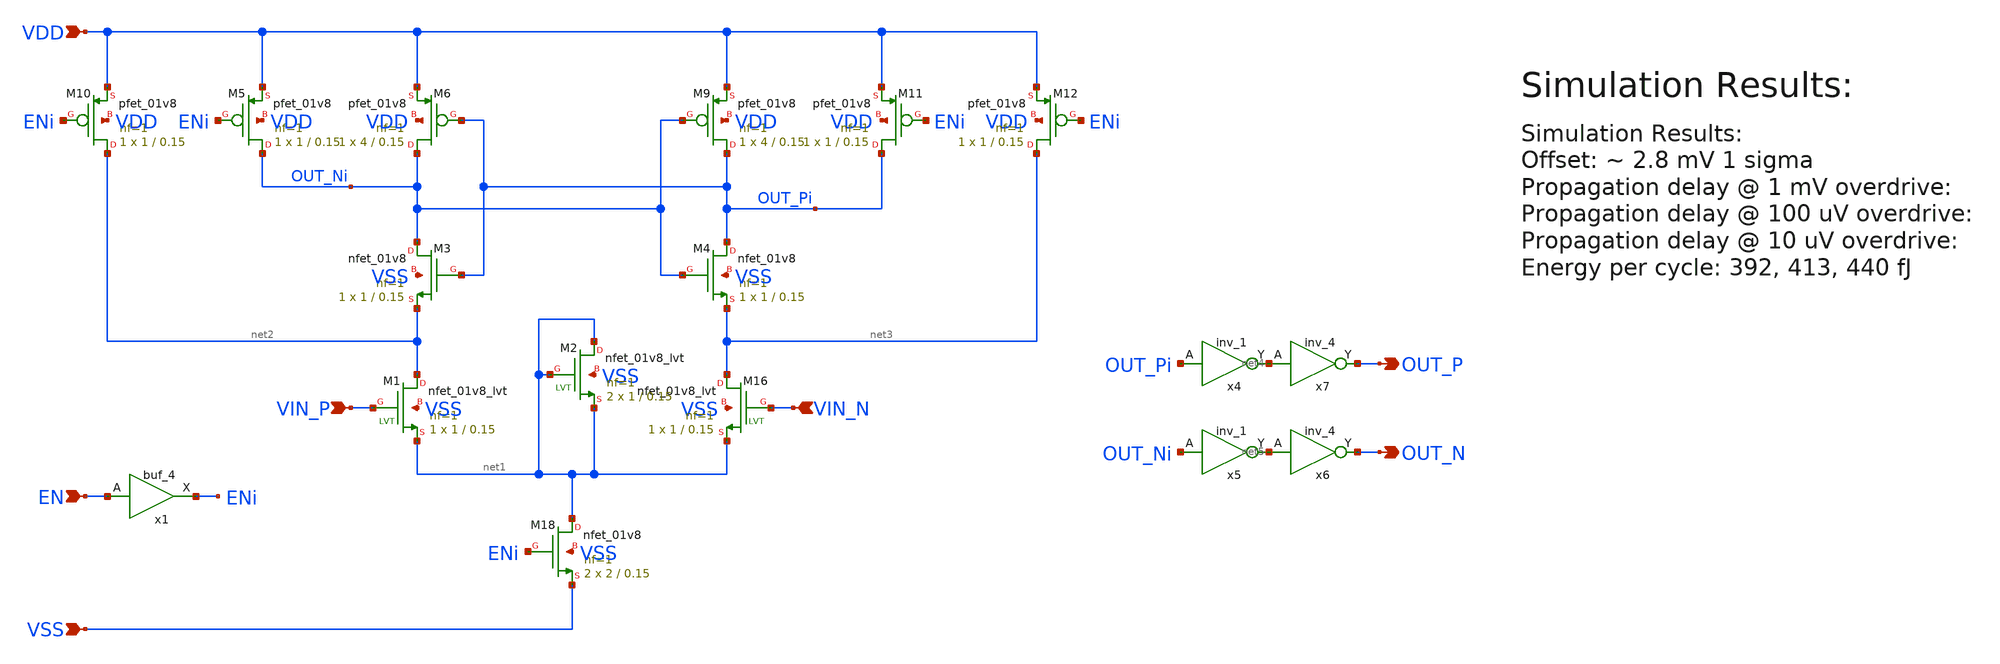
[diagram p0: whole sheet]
** sch_path: schematic/subcells/latched_comparator/latched_comparator.sch
**.subckt latched_comparator VIN_P VIN_N VDD VSS EN OUT_N OUT_P
*.ipin VIN_P
*.ipin VIN_N
*.ipin VDD
*.ipin VSS
*.ipin EN
*.opin OUT_N
*.opin OUT_P
x1 EN VSS VSS VDD VDD ENi sky130_fd_sc_hd__buf_4
XM10 net2 ENi VDD VDD sky130_fd_pr__pfet_01v8 L=0.15 W=1 nf=1 ad='int((nf+1)/2) * W/nf * 0.29' as='int((nf+2)/2) * W/nf * 0.29'
+ pd='2*int((nf+1)/2) * (W/nf + 0.29)' ps='2*int((nf+2)/2) * (W/nf + 0.29)' nrd='0.29 / W' nrs='0.29 / W'
+ sa=0 sb=0 sd=0 mult=1 m=1
XM5 OUT_Ni ENi VDD VDD sky130_fd_pr__pfet_01v8 L=0.15 W=1 nf=1 ad='int((nf+1)/2) * W/nf * 0.29' as='int((nf+2)/2) * W/nf * 0.29'
+ pd='2*int((nf+1)/2) * (W/nf + 0.29)' ps='2*int((nf+2)/2) * (W/nf + 0.29)' nrd='0.29 / W' nrs='0.29 / W'
+ sa=0 sb=0 sd=0 mult=1 m=1
XM6 OUT_Ni OUT_Pi VDD VDD sky130_fd_pr__pfet_01v8 L=0.15 W=4 nf=1 ad='int((nf+1)/2) * W/nf * 0.29' as='int((nf+2)/2) * W/nf * 0.29'
+ pd='2*int((nf+1)/2) * (W/nf + 0.29)' ps='2*int((nf+2)/2) * (W/nf + 0.29)' nrd='0.29 / W' nrs='0.29 / W'
+ sa=0 sb=0 sd=0 mult=1 m=1
XM9 OUT_Pi OUT_Ni VDD VDD sky130_fd_pr__pfet_01v8 L=0.15 W=4 nf=1 ad='int((nf+1)/2) * W/nf * 0.29' as='int((nf+2)/2) * W/nf * 0.29'
+ pd='2*int((nf+1)/2) * (W/nf + 0.29)' ps='2*int((nf+2)/2) * (W/nf + 0.29)' nrd='0.29 / W' nrs='0.29 / W'
+ sa=0 sb=0 sd=0 mult=1 m=1
XM3 OUT_Ni OUT_Pi net2 VSS sky130_fd_pr__nfet_01v8 L=0.15 W=1 nf=1 ad='int((nf+1)/2) * W/nf * 0.29' as='int((nf+2)/2) * W/nf * 0.29'
+ pd='2*int((nf+1)/2) * (W/nf + 0.29)' ps='2*int((nf+2)/2) * (W/nf + 0.29)' nrd='0.29 / W' nrs='0.29 / W'
+ sa=0 sb=0 sd=0 mult=1 m=1
XM4 OUT_Pi OUT_Ni net3 VSS sky130_fd_pr__nfet_01v8 L=0.15 W=1 nf=1 ad='int((nf+1)/2) * W/nf * 0.29' as='int((nf+2)/2) * W/nf * 0.29'
+ pd='2*int((nf+1)/2) * (W/nf + 0.29)' ps='2*int((nf+2)/2) * (W/nf + 0.29)' nrd='0.29 / W' nrs='0.29 / W'
+ sa=0 sb=0 sd=0 mult=1 m=1
XM18 net1 ENi VSS VSS sky130_fd_pr__nfet_01v8 L=0.15 W=2 nf=1 ad='int((nf+1)/2) * W/nf * 0.29' as='int((nf+2)/2) * W/nf * 0.29'
+ pd='2*int((nf+1)/2) * (W/nf + 0.29)' ps='2*int((nf+2)/2) * (W/nf + 0.29)' nrd='0.29 / W' nrs='0.29 / W'
+ sa=0 sb=0 sd=0 mult=2 m=2
XM16 net3 VIN_N net1 VSS sky130_fd_pr__nfet_01v8_lvt L=0.15 W=1 nf=1 ad='int((nf+1)/2) * W/nf * 0.29'
+ as='int((nf+2)/2) * W/nf * 0.29' pd='2*int((nf+1)/2) * (W/nf + 0.29)' ps='2*int((nf+2)/2) * (W/nf + 0.29)'
+ nrd='0.29 / W' nrs='0.29 / W' sa=0 sb=0 sd=0 mult=1 m=1
XM1 net2 VIN_P net1 VSS sky130_fd_pr__nfet_01v8_lvt L=0.15 W=1 nf=1 ad='int((nf+1)/2) * W/nf * 0.29'
+ as='int((nf+2)/2) * W/nf * 0.29' pd='2*int((nf+1)/2) * (W/nf + 0.29)' ps='2*int((nf+2)/2) * (W/nf + 0.29)'
+ nrd='0.29 / W' nrs='0.29 / W' sa=0 sb=0 sd=0 mult=1 m=1
XM11 OUT_Pi ENi VDD VDD sky130_fd_pr__pfet_01v8 L=0.15 W=1 nf=1 ad='int((nf+1)/2) * W/nf * 0.29' as='int((nf+2)/2) * W/nf * 0.29'
+ pd='2*int((nf+1)/2) * (W/nf + 0.29)' ps='2*int((nf+2)/2) * (W/nf + 0.29)' nrd='0.29 / W' nrs='0.29 / W'
+ sa=0 sb=0 sd=0 mult=1 m=1
XM12 net3 ENi VDD VDD sky130_fd_pr__pfet_01v8 L=0.15 W=1 nf=1 ad='int((nf+1)/2) * W/nf * 0.29' as='int((nf+2)/2) * W/nf * 0.29'
+ pd='2*int((nf+1)/2) * (W/nf + 0.29)' ps='2*int((nf+2)/2) * (W/nf + 0.29)' nrd='0.29 / W' nrs='0.29 / W'
+ sa=0 sb=0 sd=0 mult=1 m=1
x4 OUT_Pi VSS VSS VDD VDD net4 sky130_fd_sc_hd__inv_1
x5 OUT_Ni VSS VSS VDD VDD net5 sky130_fd_sc_hd__inv_1
x6 net5 VSS VSS VDD VDD OUT_N sky130_fd_sc_hd__inv_4
x7 net4 VSS VSS VDD VDD OUT_P sky130_fd_sc_hd__inv_4
XM2 net1 net1 net1 VSS sky130_fd_pr__nfet_01v8_lvt L=0.15 W=1 nf=1 ad='int((nf+1)/2) * W/nf * 0.29' as='int((nf+2)/2) * W/nf * 0.29'
+ pd='2*int((nf+1)/2) * (W/nf + 0.29)' ps='2*int((nf+2)/2) * (W/nf + 0.29)' nrd='0.29 / W' nrs='0.29 / W'
+ sa=0 sb=0 sd=0 mult=2 m=2
**.ends
.end
